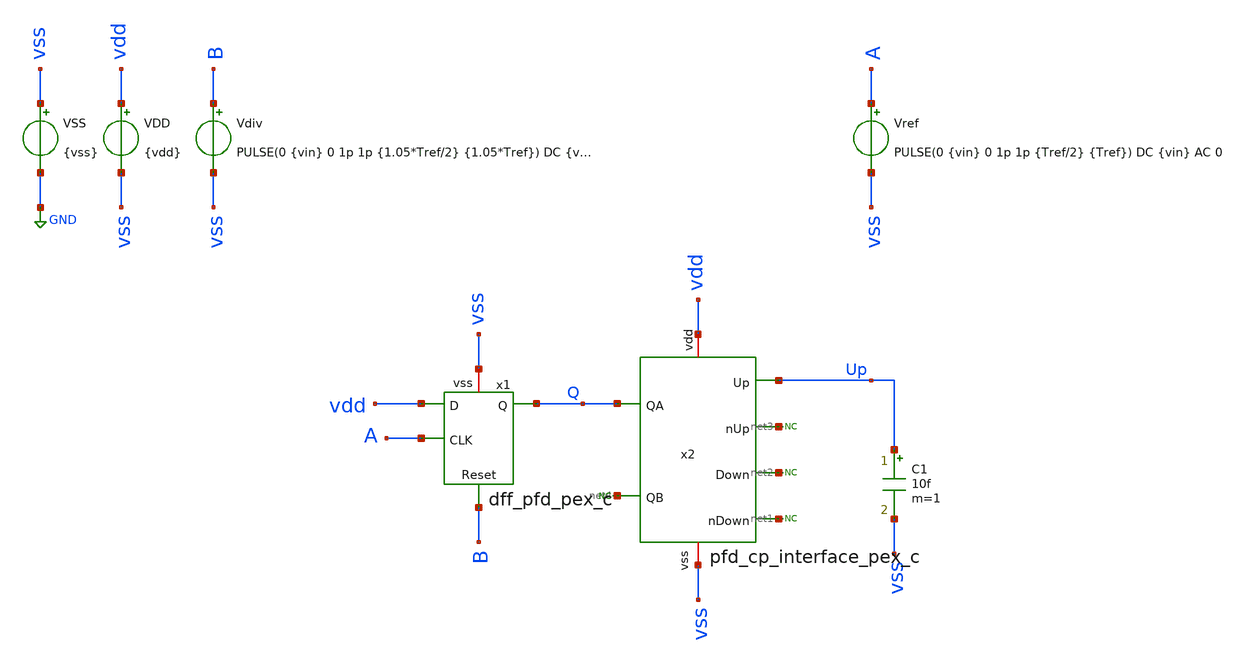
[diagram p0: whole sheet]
** sch_path: xschem/tb_DFF.sch
**.subckt tb_DFF
VSS vss GND {vss}
VDD vdd vss {vdd}
Vref A vss PULSE(0 {vin} 0 1p 1p {Tref/2} {Tref}) DC {vin} AC 0
Vdiv B vss PULSE(0 {vin} 0 1p 1p {1.05*Tref/2} {1.05*Tref}) DC {vin} AC 0
* noconn #net1
* noconn #net2
* noconn #net3
* noconn #net4
C1 Up vss 10f m=1
x2 Up vdd Q net3 net2 net4 vss net1 pfd_cp_interface_pex_c
x1 vdd A Q B vss dff_pfd_pex_c
**** begin user architecture code



* Parameters
.param kp = 0.9
.param vdd = kp*1.8
.param vss = 0.0
.param vin = 1.8
.param fref = 100e6
.param Tref = 1/fref
.param C = 1f

.options TEMP = 50.0

* Models
.lib ~/skywater/skywater-pdk/libraries/sky130_fd_pr_ngspice/latest/models/corners/sky130.lib SS
.include ~/caravel_analog_fulgor/xschem/simulations/pfd_cp_interface_pex_c.spice
.include ~/caravel_analog_fulgor/xschem/simulations/dff_pfd_pex_c.spice

.ic v(net3) = 0.0
.ic v(net4) = 0.0
.ic v(Q) = 0.0

* Data to save
.save all

* Simulation
.control
	tran 0.1ns 200ns
	*meas tran Tosc trig v(out) val=0.9 fall=5 targ v(out) val=0.9 fall=15
	*meas tran Td1  trig v(out) val=0.9 fall=5 targ v(out1) val=0.9 rise=6
	*meas tran Td2  trig v(out1) val=0.9 fall=5 targ v(out2) val=0.9 rise=6
	*meas tran Td3  trig v(out2) val=0.9 fall=5 targ v(out) val=0.9 rise=5
	*let  T = Tosc/10.0
	*let  f = 1/T
	*let Td = 1/(2*3*f)
	*print T f Td
	write tb_DFF_nor_tran.raw
	plot v(A)+2 v(B)+2 v(Q)
.endc

.end


**** end user architecture code
**.ends
.GLOBAL GND
.end
